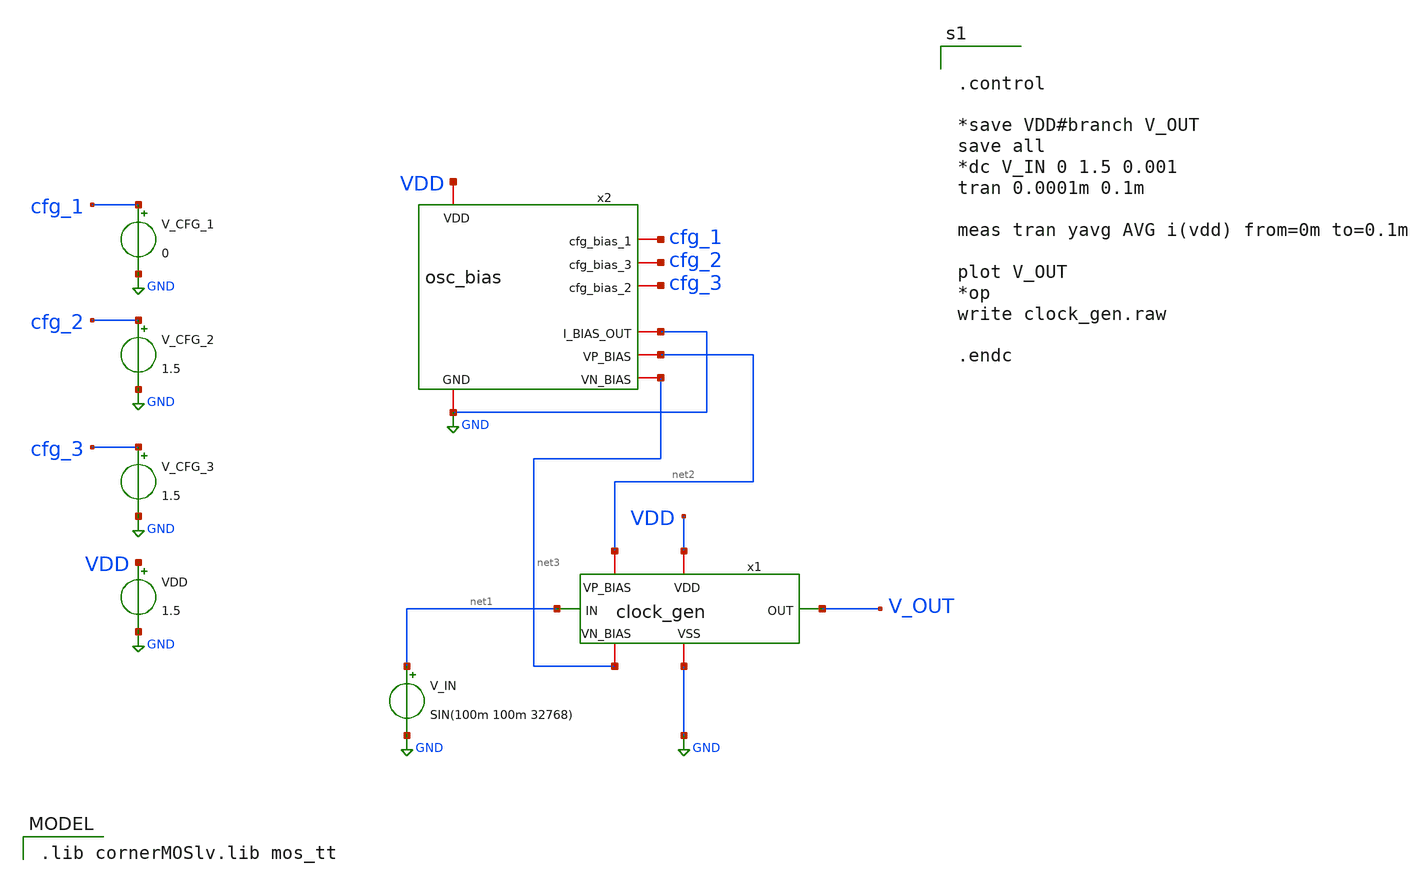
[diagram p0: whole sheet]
** sch_path: clock_gen_tb.sch
**.subckt clock_gen_tb
VDD VDD GND 1.5
V_IN net1 GND SIN(100m 100m 32768)
x1 VDD net1 V_OUT GND net2 net3 clock_gen
x2 VDD cfg_1 cfg_2 cfg_3 GND GND net2 net3 osc_bias
V_CFG_1 cfg_1 GND 0
V_CFG_2 cfg_2 GND 1.5
V_CFG_3 cfg_3 GND 1.5
**** begin user architecture code
 .lib cornerMOSlv.lib mos_tt



.control

*save VDD#branch V_OUT
save all
*dc V_IN 0 1.5 0.001
tran 0.0001m 0.1m

meas tran yavg AVG i(vdd) from=0m to=0.1m

plot V_OUT
*op
write clock_gen.raw

.endc


**** end user architecture code
**.ends

* expanding   symbol:  clock_gen.sym # of pins=6
** sym_path: clock_gen.sym
** sch_path: clock_gen.sch
.subckt clock_gen VDD IN OUT VSS VP_BIAS VN_BIAS
*.ipin IN
*.iopin VSS
*.opin OUT
*.iopin VDD
*.ipin VP_BIAS
*.ipin VN_BIAS
XM13 V_OUT_1 V_IN_1 net2 VSS sg13_lv_nmos w={w_p} l={l_p} ng=1 m=1 mm_ok=1
XM14 V_OUT_1 V_IN_1 M2_Source VDD sg13_lv_pmos w={2*{w_p}} l={l_p} ng=1 m=1 mm_ok=1
XM15 net3 VN_BIAS VSS VSS sg13_lv_nmos w={w_p} l={l_p} ng=1 m=1 mm_ok=1
XM16 net1 VP_BIAS VDD VDD sg13_lv_pmos w={2*{w_p}} l={l_p} ng=1 m=1 mm_ok=1
Vmeas_PMOS1 net1 M2_Source 0
.save i(vmeas_pmos1)
Vmeas_NMOS1 net2 net3 0
.save i(vmeas_nmos1)
C2 IN V_IN_1 50p m=1
XM17 V_OUT_2 V_OUT_1 net4 VSS sg13_lv_nmos w={w_p} l={l_p} ng=1 m=1 mm_ok=1
XM18 V_OUT_2 V_OUT_1 net6 VDD sg13_lv_pmos w={2*{w_p}} l={l_p} ng=1 m=1 mm_ok=1
Vmeas_NMOS2 net4 net7 0
.save i(vmeas_nmos2)
XM19 net5 VP_BIAS VDD VDD sg13_lv_pmos w={2*{w_p}} l={l_p} ng=1 m=1 mm_ok=1
Vmeas_PMOS2 net5 net6 0
.save i(vmeas_pmos2)
XM20 net7 VN_BIAS VSS VSS sg13_lv_nmos w={w_p} l={l_p} ng=1 m=1 mm_ok=1
XM21 OUT V_OUT_4 net10 VSS sg13_lv_nmos w={w_p} l={l_p} ng=1 m=1 mm_ok=1
XM22 OUT V_OUT_4 net9 VDD sg13_lv_pmos w={2*{w_p}} l={l_p} ng=1 m=1 mm_ok=1
XM23 V_OUT_1 net8 net8 net8 sg13_lv_pmos w=0.5u l=2u ng=1 m=1 mm_ok=1
XM24 net8 V_IN_1 V_IN_1 V_IN_1 sg13_lv_pmos w=0.5u l=2u ng=1 m=1 mm_ok=1
Vmeas_PMOS_OUT VDD net9 0
.save i(vmeas_pmos_out)
Vmeas_NMOS_OUT net10 VSS 0
.save i(vmeas_nmos_out)
XM25 V_OUT_3 V_OUT_2 net11 VSS sg13_lv_nmos w={w_p} l={l_p} ng=1 m=1 mm_ok=1
XM26 V_OUT_3 V_OUT_2 net13 VDD sg13_lv_pmos w={2*{w_p}} l={l_p} ng=1 m=1 mm_ok=1
Vmeas_NMOS3 net11 net14 0
.save i(vmeas_nmos3)
XM27 net12 VP_BIAS VDD VDD sg13_lv_pmos w={2*{w_p}} l={l_p} ng=1 m=1 mm_ok=1
Vmeas_PMOS3 net12 net13 0
.save i(vmeas_pmos3)
XM28 net14 VN_BIAS VSS VSS sg13_lv_nmos w={w_p} l={l_p} ng=1 m=1 mm_ok=1
XM29 V_OUT_4 V_OUT_3 net15 VSS sg13_lv_nmos w={w_p} l={l_p} ng=1 m=1 mm_ok=1
XM30 V_OUT_4 V_OUT_3 net17 VDD sg13_lv_pmos w={2*{w_p}} l={l_p} ng=1 m=1 mm_ok=1
Vmeas_NMOS4 net15 net18 0
.save i(vmeas_nmos4)
XM31 net16 VP_BIAS VDD VDD sg13_lv_pmos w={2*{w_p}} l={l_p} ng=1 m=1 mm_ok=1
Vmeas_PMOS4 net16 net17 0
.save i(vmeas_pmos4)
XM32 net18 VN_BIAS VSS VSS sg13_lv_nmos w={w_p} l={l_p} ng=1 m=1 mm_ok=1
.ends


* expanding   symbol:  osc_bias.sym # of pins=8
** sym_path: osc_bias.sym
** sch_path: osc_bias.sch
.subckt osc_bias VDD cfg_bias_1 cfg_bias_3 cfg_bias_2 GND I_BIAS_OUT VP_BIAS VN_BIAS
*.iopin VDD
*.iopin GND
*.iopin I_BIAS_OUT
*.iopin cfg_bias_1
*.iopin cfg_bias_2
*.iopin cfg_bias_3
*.opin VN_BIAS
*.opin VP_BIAS
XM1 net1 net1 VDD VDD sg13_lv_pmos w=0.25u l=10u ng=1 m=1 mm_ok=1
XM3 net1 net1 net2 GND sg13_lv_nmos w=0.25u l=10u ng=1 m=1 mm_ok=1
XM4 net2 net2 net3 GND sg13_lv_nmos w=0.25u l=10u ng=1 m=1 mm_ok=1
XM5 net3 net3 net14 GND sg13_lv_nmos w=0.25u l=10u ng=1 m=1 mm_ok=1
XM2 net9 net1 VDD VDD sg13_lv_pmos w=0.25u l=10u ng=1 m=2 mm_ok=1
XM6 net4 cfg_bias_1 net9 VDD sg13_lv_pmos w=0.25u l=10u ng=1 m=1 mm_ok=1
XM7 net5 net1 VDD VDD sg13_lv_pmos w=0.25u l=10u ng=1 m=4 mm_ok=1
XM8 net6 net1 VDD VDD sg13_lv_pmos w=0.25u l=10u ng=1 m=20 mm_ok=1
XM9 net4 cfg_bias_2 net5 VDD sg13_lv_pmos w=0.5u l=10u ng=1 m=1 mm_ok=1
XM10 net4 cfg_bias_3 net6 VDD sg13_lv_pmos w=1u l=10u ng=1 m=1 mm_ok=1
XM11 net7 net7 net8 GND sg13_lv_nmos w=0.2u l=10u ng=1 m=1 mm_ok=1
Vmeas net8 GND 0
.save i(vmeas)
XM12 VP_BIAS VP_BIAS net12 VDD sg13_lv_pmos w=0.8u l=0.13u ng=1 m=1 mm_ok=1
XM13 VN_BIAS VN_BIAS net11 GND sg13_lv_nmos w=0.4u l=0.13u ng=1 m=1 mm_ok=1
Vmeas1 VDD net12 0
.save i(vmeas1)
Vmeas2 net11 GND 0
.save i(vmeas2)
XM14 net10 net10 VN_BIAS GND sg13_lv_nmos w=0.4u l=10u ng=1 m=1 mm_ok=1
XM15 net13 net13 net10 GND sg13_lv_nmos w=0.4u l=10u ng=1 m=1 mm_ok=1
XM16 VP_BIAS VP_BIAS net13 GND sg13_lv_nmos w=0.4u l=10u ng=1 m=1 mm_ok=1
XM17 net14 net14 net7 GND sg13_lv_nmos w=0.25u l=10u ng=1 m=1 mm_ok=1
Vmeas3 net4 I_BIAS_OUT 0
.save i(vmeas3)
.ends

.GLOBAL GND
.end
